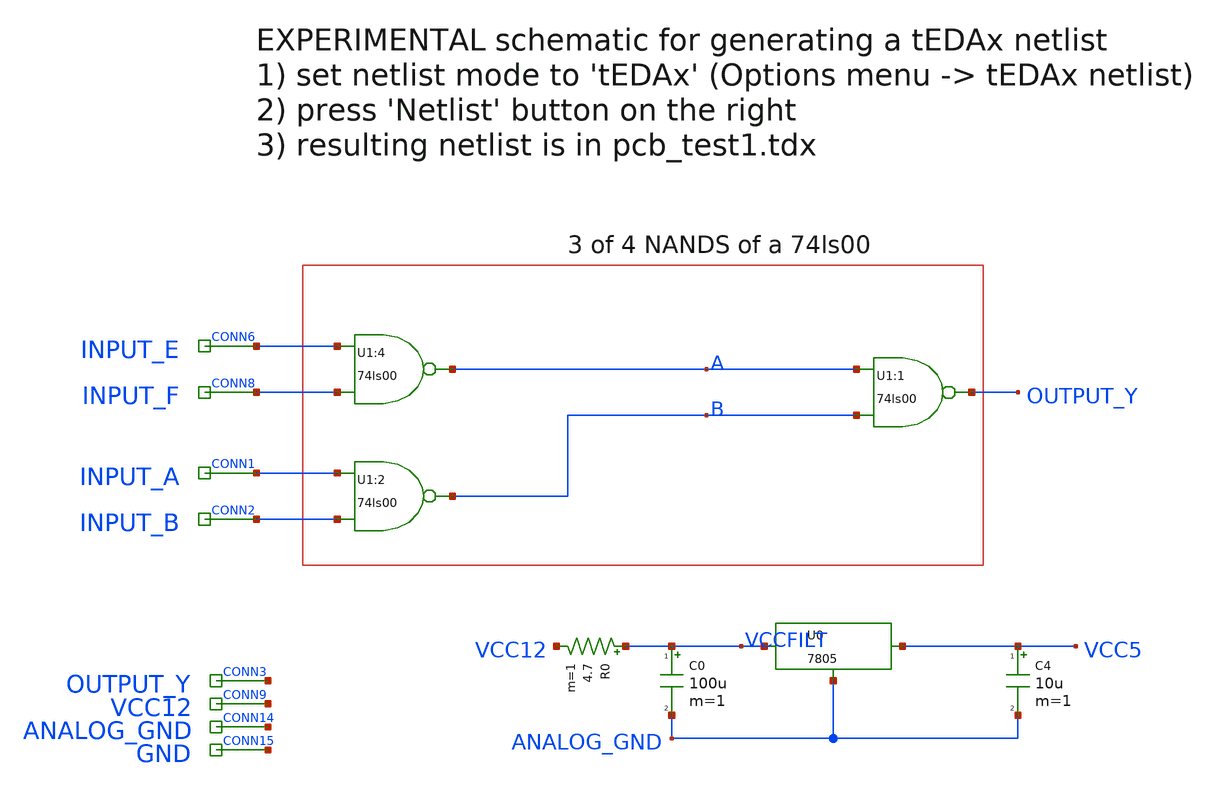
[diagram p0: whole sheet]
** sch_path: library/pcb/pcb_test1.sch
**.subckt pcb_test1 INPUT_A INPUT_B OUTPUT_Y INPUT_E INPUT_F VCC12 ANALOG_GND GND
*.ipin INPUT_A
*.ipin INPUT_B
*.ipin OUTPUT_Y
*.ipin INPUT_E
*.ipin INPUT_F
*.ipin VCC12
*.ipin ANALOG_GND
*.ipin GND
C0 VCCFILT ANALOG_GND 100u m=1
xU0 VCCFILT ANALOG_GND VCC5 r7805
C4 VCC5 ANALOG_GND 10u m=1
R0 VCCFILT VCC12 4.7 m=1
**.ends
.end
